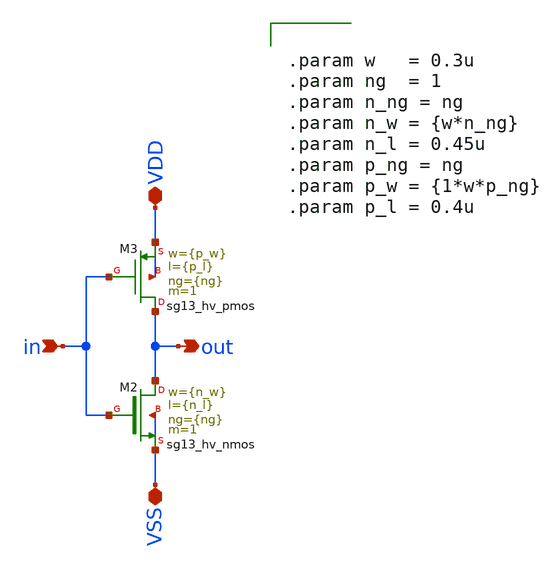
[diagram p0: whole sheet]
** sch_path: macros/heichips26_vcr/macros/switched_capacitor/schematic/xschem/hv_inverter_0u3.sch
**.subckt hv_inverter_0u3 in VDD VSS out
*.ipin in
*.iopin VDD
*.iopin VSS
*.opin out
XM2 out in VSS VSS sg13_hv_nmos w={n_w} l={n_l} ng={ng} m=1 mm_ok=1
XM3 out in VDD VDD sg13_hv_pmos w={p_w} l={p_l} ng={ng} m=1 mm_ok=1
**** begin user architecture code


.param w   = 0.3u
.param ng  = 1
.param n_ng = ng
.param n_w = {w*n_ng}
.param n_l = 0.45u
.param p_ng = ng
.param p_w = {1*w*p_ng}
.param p_l = 0.4u


**** end user architecture code
**.ends
.end
